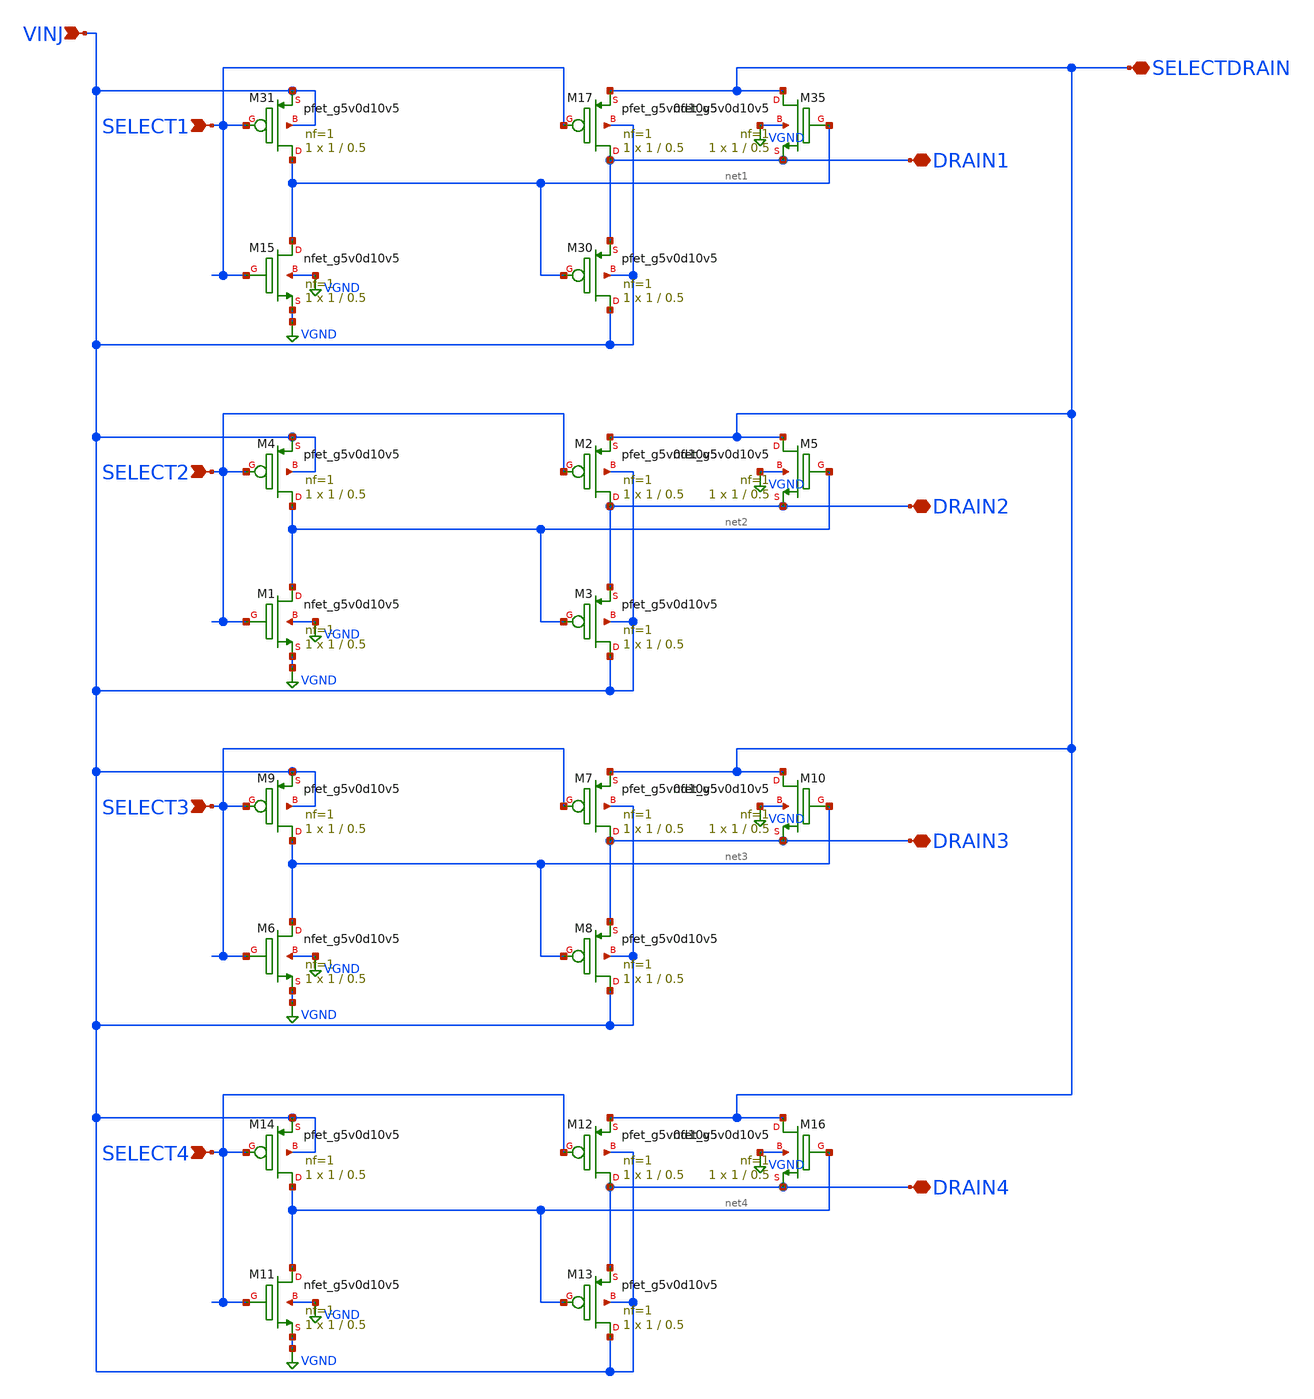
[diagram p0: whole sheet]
** sch_path: libs.ref/sky130_hilas_sc/xschem/sky130_hilas_drainSelect01.sch
**.subckt sky130_hilas_drainSelect01 SELECT1 SELECTDRAIN DRAIN1 VINJ SELECT2 DRAIN2 SELECT3 DRAIN3
*+ SELECT4 DRAIN4
*.ipin SELECT1
*.iopin SELECTDRAIN
*.iopin DRAIN1
*.ipin VINJ
*.ipin SELECT2
*.iopin DRAIN2
*.ipin SELECT3
*.iopin DRAIN3
*.ipin SELECT4
*.iopin DRAIN4
XM15 net1 SELECT1 VGND VGND sky130_fd_pr__nfet_g5v0d10v5 L=0.5 W=1 nf=1 ad='int((nf+1)/2) * W/nf * 0.29'
+ as='int((nf+2)/2) * W/nf * 0.29' pd='2*int((nf+1)/2) * (W/nf + 0.29)' ps='2*int((nf+2)/2) * (W/nf + 0.29)'
+ nrd='0.29 / W' nrs='0.29 / W' sa=0 sb=0 sd=0 mult=1 m=1
XM17 DRAIN1 SELECT1 SELECTDRAIN VINJ sky130_fd_pr__pfet_g5v0d10v5 L=0.5 W=1 nf=1 ad='int((nf+1)/2) * W/nf * 0.29'
+ as='int((nf+2)/2) * W/nf * 0.29' pd='2*int((nf+1)/2) * (W/nf + 0.29)' ps='2*int((nf+2)/2) * (W/nf + 0.29)'
+ nrd='0.29 / W' nrs='0.29 / W' sa=0 sb=0 sd=0 mult=1 m=1
XM30 VINJ net1 DRAIN1 VINJ sky130_fd_pr__pfet_g5v0d10v5 L=0.5 W=1 nf=1 ad='int((nf+1)/2) * W/nf * 0.29'
+ as='int((nf+2)/2) * W/nf * 0.29' pd='2*int((nf+1)/2) * (W/nf + 0.29)' ps='2*int((nf+2)/2) * (W/nf + 0.29)'
+ nrd='0.29 / W' nrs='0.29 / W' sa=0 sb=0 sd=0 mult=1 m=1
XM31 net1 SELECT1 VINJ VINJ sky130_fd_pr__pfet_g5v0d10v5 L=0.5 W=1 nf=1 ad='int((nf+1)/2) * W/nf * 0.29'
+ as='int((nf+2)/2) * W/nf * 0.29' pd='2*int((nf+1)/2) * (W/nf + 0.29)' ps='2*int((nf+2)/2) * (W/nf + 0.29)'
+ nrd='0.29 / W' nrs='0.29 / W' sa=0 sb=0 sd=0 mult=1 m=1
XM35 SELECTDRAIN net1 DRAIN1 VGND sky130_fd_pr__nfet_g5v0d10v5 L=0.5 W=1 nf=1 ad='int((nf+1)/2) * W/nf * 0.29'
+ as='int((nf+2)/2) * W/nf * 0.29' pd='2*int((nf+1)/2) * (W/nf + 0.29)' ps='2*int((nf+2)/2) * (W/nf + 0.29)'
+ nrd='0.29 / W' nrs='0.29 / W' sa=0 sb=0 sd=0 mult=1 m=1
XM1 net2 SELECT2 VGND VGND sky130_fd_pr__nfet_g5v0d10v5 L=0.5 W=1 nf=1 ad='int((nf+1)/2) * W/nf * 0.29'
+ as='int((nf+2)/2) * W/nf * 0.29' pd='2*int((nf+1)/2) * (W/nf + 0.29)' ps='2*int((nf+2)/2) * (W/nf + 0.29)'
+ nrd='0.29 / W' nrs='0.29 / W' sa=0 sb=0 sd=0 mult=1 m=1
XM2 DRAIN2 SELECT2 SELECTDRAIN VINJ sky130_fd_pr__pfet_g5v0d10v5 L=0.5 W=1 nf=1 ad='int((nf+1)/2) * W/nf * 0.29'
+ as='int((nf+2)/2) * W/nf * 0.29' pd='2*int((nf+1)/2) * (W/nf + 0.29)' ps='2*int((nf+2)/2) * (W/nf + 0.29)'
+ nrd='0.29 / W' nrs='0.29 / W' sa=0 sb=0 sd=0 mult=1 m=1
XM3 VINJ net2 DRAIN2 VINJ sky130_fd_pr__pfet_g5v0d10v5 L=0.5 W=1 nf=1 ad='int((nf+1)/2) * W/nf * 0.29'
+ as='int((nf+2)/2) * W/nf * 0.29' pd='2*int((nf+1)/2) * (W/nf + 0.29)' ps='2*int((nf+2)/2) * (W/nf + 0.29)'
+ nrd='0.29 / W' nrs='0.29 / W' sa=0 sb=0 sd=0 mult=1 m=1
XM4 net2 SELECT2 VINJ VINJ sky130_fd_pr__pfet_g5v0d10v5 L=0.5 W=1 nf=1 ad='int((nf+1)/2) * W/nf * 0.29'
+ as='int((nf+2)/2) * W/nf * 0.29' pd='2*int((nf+1)/2) * (W/nf + 0.29)' ps='2*int((nf+2)/2) * (W/nf + 0.29)'
+ nrd='0.29 / W' nrs='0.29 / W' sa=0 sb=0 sd=0 mult=1 m=1
XM5 SELECTDRAIN net2 DRAIN2 VGND sky130_fd_pr__nfet_g5v0d10v5 L=0.5 W=1 nf=1 ad='int((nf+1)/2) * W/nf * 0.29'
+ as='int((nf+2)/2) * W/nf * 0.29' pd='2*int((nf+1)/2) * (W/nf + 0.29)' ps='2*int((nf+2)/2) * (W/nf + 0.29)'
+ nrd='0.29 / W' nrs='0.29 / W' sa=0 sb=0 sd=0 mult=1 m=1
XM6 net3 SELECT3 VGND VGND sky130_fd_pr__nfet_g5v0d10v5 L=0.5 W=1 nf=1 ad='int((nf+1)/2) * W/nf * 0.29'
+ as='int((nf+2)/2) * W/nf * 0.29' pd='2*int((nf+1)/2) * (W/nf + 0.29)' ps='2*int((nf+2)/2) * (W/nf + 0.29)'
+ nrd='0.29 / W' nrs='0.29 / W' sa=0 sb=0 sd=0 mult=1 m=1
XM7 DRAIN3 SELECT3 SELECTDRAIN VINJ sky130_fd_pr__pfet_g5v0d10v5 L=0.5 W=1 nf=1 ad='int((nf+1)/2) * W/nf * 0.29'
+ as='int((nf+2)/2) * W/nf * 0.29' pd='2*int((nf+1)/2) * (W/nf + 0.29)' ps='2*int((nf+2)/2) * (W/nf + 0.29)'
+ nrd='0.29 / W' nrs='0.29 / W' sa=0 sb=0 sd=0 mult=1 m=1
XM8 VINJ net3 DRAIN3 VINJ sky130_fd_pr__pfet_g5v0d10v5 L=0.5 W=1 nf=1 ad='int((nf+1)/2) * W/nf * 0.29'
+ as='int((nf+2)/2) * W/nf * 0.29' pd='2*int((nf+1)/2) * (W/nf + 0.29)' ps='2*int((nf+2)/2) * (W/nf + 0.29)'
+ nrd='0.29 / W' nrs='0.29 / W' sa=0 sb=0 sd=0 mult=1 m=1
XM9 net3 SELECT3 VINJ VINJ sky130_fd_pr__pfet_g5v0d10v5 L=0.5 W=1 nf=1 ad='int((nf+1)/2) * W/nf * 0.29'
+ as='int((nf+2)/2) * W/nf * 0.29' pd='2*int((nf+1)/2) * (W/nf + 0.29)' ps='2*int((nf+2)/2) * (W/nf + 0.29)'
+ nrd='0.29 / W' nrs='0.29 / W' sa=0 sb=0 sd=0 mult=1 m=1
XM10 SELECTDRAIN net3 DRAIN3 VGND sky130_fd_pr__nfet_g5v0d10v5 L=0.5 W=1 nf=1 ad='int((nf+1)/2) * W/nf * 0.29'
+ as='int((nf+2)/2) * W/nf * 0.29' pd='2*int((nf+1)/2) * (W/nf + 0.29)' ps='2*int((nf+2)/2) * (W/nf + 0.29)'
+ nrd='0.29 / W' nrs='0.29 / W' sa=0 sb=0 sd=0 mult=1 m=1
XM11 net4 SELECT4 VGND VGND sky130_fd_pr__nfet_g5v0d10v5 L=0.5 W=1 nf=1 ad='int((nf+1)/2) * W/nf * 0.29'
+ as='int((nf+2)/2) * W/nf * 0.29' pd='2*int((nf+1)/2) * (W/nf + 0.29)' ps='2*int((nf+2)/2) * (W/nf + 0.29)'
+ nrd='0.29 / W' nrs='0.29 / W' sa=0 sb=0 sd=0 mult=1 m=1
XM12 DRAIN4 SELECT4 SELECTDRAIN VINJ sky130_fd_pr__pfet_g5v0d10v5 L=0.5 W=1 nf=1 ad='int((nf+1)/2) * W/nf * 0.29'
+ as='int((nf+2)/2) * W/nf * 0.29' pd='2*int((nf+1)/2) * (W/nf + 0.29)' ps='2*int((nf+2)/2) * (W/nf + 0.29)'
+ nrd='0.29 / W' nrs='0.29 / W' sa=0 sb=0 sd=0 mult=1 m=1
XM13 VINJ net4 DRAIN4 VINJ sky130_fd_pr__pfet_g5v0d10v5 L=0.5 W=1 nf=1 ad='int((nf+1)/2) * W/nf * 0.29'
+ as='int((nf+2)/2) * W/nf * 0.29' pd='2*int((nf+1)/2) * (W/nf + 0.29)' ps='2*int((nf+2)/2) * (W/nf + 0.29)'
+ nrd='0.29 / W' nrs='0.29 / W' sa=0 sb=0 sd=0 mult=1 m=1
XM14 net4 SELECT4 VINJ VINJ sky130_fd_pr__pfet_g5v0d10v5 L=0.5 W=1 nf=1 ad='int((nf+1)/2) * W/nf * 0.29'
+ as='int((nf+2)/2) * W/nf * 0.29' pd='2*int((nf+1)/2) * (W/nf + 0.29)' ps='2*int((nf+2)/2) * (W/nf + 0.29)'
+ nrd='0.29 / W' nrs='0.29 / W' sa=0 sb=0 sd=0 mult=1 m=1
XM16 SELECTDRAIN net4 DRAIN4 VGND sky130_fd_pr__nfet_g5v0d10v5 L=0.5 W=1 nf=1 ad='int((nf+1)/2) * W/nf * 0.29'
+ as='int((nf+2)/2) * W/nf * 0.29' pd='2*int((nf+1)/2) * (W/nf + 0.29)' ps='2*int((nf+2)/2) * (W/nf + 0.29)'
+ nrd='0.29 / W' nrs='0.29 / W' sa=0 sb=0 sd=0 mult=1 m=1
**.ends
.GLOBAL VGND
.end
